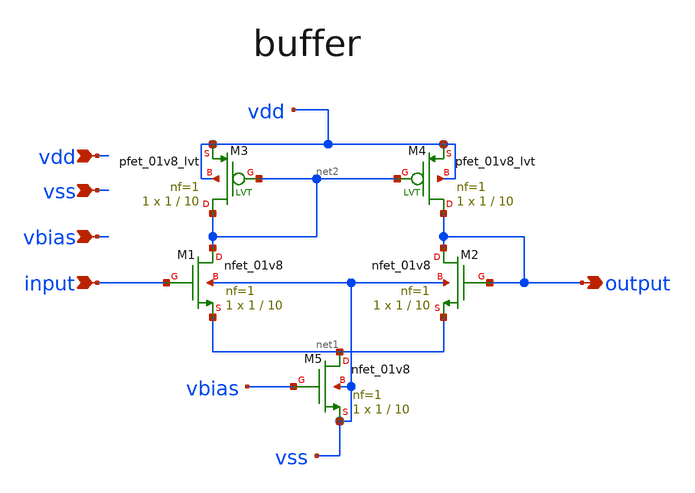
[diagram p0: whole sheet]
** sch_path: xschem/buffer.sch
**.subckt buffer output input vdd vss vbias
*.opin output
*.ipin input
*.ipin vdd
*.ipin vss
*.ipin vbias
XM1 net2 input net1 vss sky130_fd_pr__nfet_01v8 L=10 W=1 nf=1 ad='int((nf+1)/2) * W/nf * 0.29' as='int((nf+2)/2) * W/nf * 0.29'
+ pd='2*int((nf+1)/2) * (W/nf + 0.29)' ps='2*int((nf+2)/2) * (W/nf + 0.29)' nrd='0.29 / W' nrs='0.29 / W'
+ sa=0 sb=0 sd=0 mult=1 m=1
XM2 output output net1 vss sky130_fd_pr__nfet_01v8 L=10 W=1 nf=1 ad='int((nf+1)/2) * W/nf * 0.29' as='int((nf+2)/2) * W/nf * 0.29'
+ pd='2*int((nf+1)/2) * (W/nf + 0.29)' ps='2*int((nf+2)/2) * (W/nf + 0.29)' nrd='0.29 / W' nrs='0.29 / W'
+ sa=0 sb=0 sd=0 mult=1 m=1
XM5 net1 vbias vss vss sky130_fd_pr__nfet_01v8 L=10 W=1 nf=1 ad='int((nf+1)/2) * W/nf * 0.29' as='int((nf+2)/2) * W/nf * 0.29'
+ pd='2*int((nf+1)/2) * (W/nf + 0.29)' ps='2*int((nf+2)/2) * (W/nf + 0.29)' nrd='0.29 / W' nrs='0.29 / W'
+ sa=0 sb=0 sd=0 mult=1 m=1
XM4 output net2 vdd vdd sky130_fd_pr__pfet_01v8_lvt L=10 W=1 nf=1 ad='int((nf+1)/2) * W/nf * 0.29' as='int((nf+2)/2) * W/nf * 0.29'
+ pd='2*int((nf+1)/2) * (W/nf + 0.29)' ps='2*int((nf+2)/2) * (W/nf + 0.29)' nrd='0.29 / W' nrs='0.29 / W'
+ sa=0 sb=0 sd=0 mult=1 m=1
XM3 net2 net2 vdd vdd sky130_fd_pr__pfet_01v8_lvt L=10 W=1 nf=1 ad='int((nf+1)/2) * W/nf * 0.29' as='int((nf+2)/2) * W/nf * 0.29'
+ pd='2*int((nf+1)/2) * (W/nf + 0.29)' ps='2*int((nf+2)/2) * (W/nf + 0.29)' nrd='0.29 / W' nrs='0.29 / W'
+ sa=0 sb=0 sd=0 mult=1 m=1
**.ends
.end
